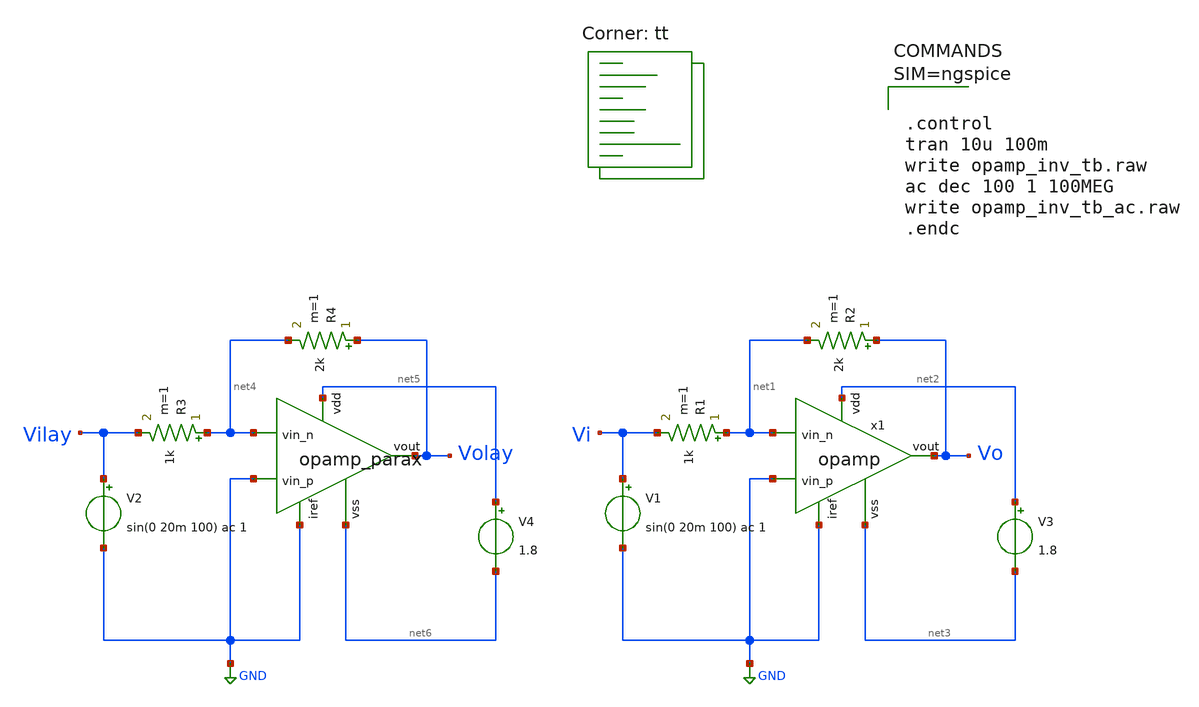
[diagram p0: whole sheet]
** sch_path: xschem/opamp_inv_tb.sch
**.subckt opamp_inv_tb
x1 net2 GND net1 GND Vo net3 opamp
R1 net1 Vi 1k m=1
R2 Vo net1 2k m=1
V1 Vi GND sin(0 20m 100) ac 1
V3 net2 net3 1.8
x1 net5 GND net4 GND Volay net6 opamp_parax
R3 net4 Vilay 1k m=1
R4 Volay net4 2k m=1
V2 Vilay GND sin(0 20m 100) ac 1
V4 net5 net6 1.8
**** begin user architecture code



.control
tran 10u 100m
write opamp_inv_tb.raw
ac dec 100 1 100MEG
write opamp_inv_tb_ac.raw
.endc



.lib $::SKYWATER_MODELS/sky130.lib.spice tt
**** end user architecture code
**.ends
.GLOBAL GND
.end
